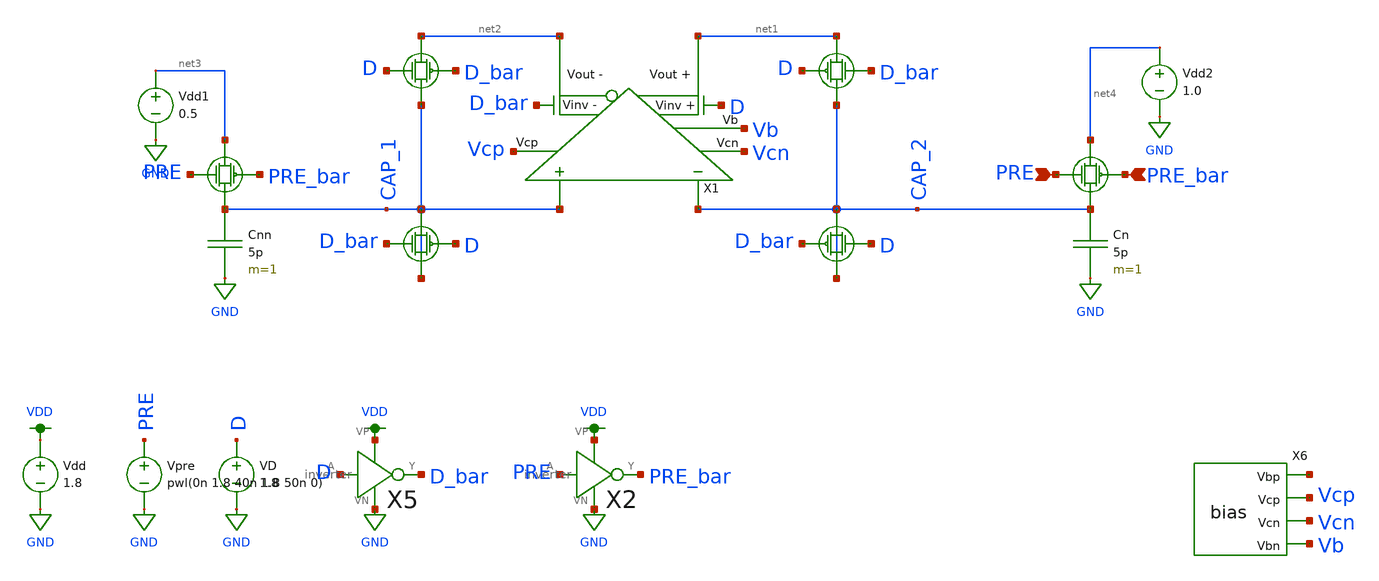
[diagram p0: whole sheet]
** sch_path: simulations/bre_sim.sch
**.subckt bre_sim PRE_bar PRE
*.ipin PRE_bar
*.ipin PRE
X1 D_bar net1 net2 Vcp Vb CAP_2 CAP_1 D Vcn ota W_U=12 L_U=0.5
Cn CAP_2 GND 5p m=1
Cnn CAP_1 GND 5p m=1
Vdd VDD GND 1.8
Vpre PRE GND pwl(0n 1.8 40n 1.8 50n 0)
X2 PRE PRE_bar VDD GND inverter
X5 D D_bar VDD GND inverter
VD D GND 1.8
X6 net5 Vcp Vcn Vb bias
Vdd1 net3 GND 0.5
Vdd2 net4 GND 1.0
**** begin user architecture code

.option wnflag=1
.param MC_SWITCH=0.0
.lib ~/skywater/skywater-pdk/libraries/sky130_fd_pr_ngspice/latest/models/sky130.lib.spice tt


.tran 0.1n 10u
.save all

**** end user architecture code
**.ends

* expanding   symbol:  ../schematics/ota.sym # of pins=9
** sym_path: schematics/ota.sym
** sch_path: schematics/ota.sch
.subckt ota Vinv_n Vout_p Vout_n Vcp Vb Vin_n Vin_p Vinv_p Vcn  L_U=0.5 W_U=12
*.ipin Vin_n
*.ipin Vin_p
*.opin Vout_n
*.opin Vout_p
*.ipin Vcp
*.ipin Vb
*.ipin Vinv_p
*.ipin Vinv_n
*.ipin Vcn
XM18 net3 net3 VDD VDD sky130_fd_pr__pfet_01v8 L=L_U W=W_U nf=1 ad='int((nf+1)/2) * W/nf * 0.29' as='int((nf+2)/2) * W/nf * 0.29'
+ pd='2*int((nf+1)/2) * (W/nf + 0.29)' ps='2*int((nf+2)/2) * (W/nf + 0.29)' nrd='0.29 / W' nrs='0.29 / W'
+ sa=0 sb=0 sd=0 mult=1 m=1
XM19 net4 Vin_n net1 GND sky130_fd_pr__nfet_01v8 L=L_U W=W_U nf=1 ad='int((nf+1)/2) * W/nf * 0.29' as='int((nf+2)/2) * W/nf * 0.29'
+ pd='2*int((nf+1)/2) * (W/nf + 0.29)' ps='2*int((nf+2)/2) * (W/nf + 0.29)' nrd='0.29 / W' nrs='0.29 / W'
+ sa=0 sb=0 sd=0 mult=1 m=1
XM20 net3 Vin_p net1 GND sky130_fd_pr__nfet_01v8 L=L_U W=W_U nf=1 ad='int((nf+1)/2) * W/nf * 0.29' as='int((nf+2)/2) * W/nf * 0.29'
+ pd='2*int((nf+1)/2) * (W/nf + 0.29)' ps='2*int((nf+2)/2) * (W/nf + 0.29)' nrd='0.29 / W' nrs='0.29 / W'
+ sa=0 sb=0 sd=0 mult=1 m=1
XM21 net1 Vb GND GND sky130_fd_pr__nfet_01v8 L=L_U W=W_U nf=1 ad='int((nf+1)/2) * W/nf * 0.29' as='int((nf+2)/2) * W/nf * 0.29'
+ pd='2*int((nf+1)/2) * (W/nf + 0.29)' ps='2*int((nf+2)/2) * (W/nf + 0.29)' nrd='0.29 / W' nrs='0.29 / W'
+ sa=0 sb=0 sd=0 mult=1 m=1
XM22 net4 net4 VDD VDD sky130_fd_pr__pfet_01v8 L=L_U W=W_U nf=1 ad='int((nf+1)/2) * W/nf * 0.29' as='int((nf+2)/2) * W/nf * 0.29'
+ pd='2*int((nf+1)/2) * (W/nf + 0.29)' ps='2*int((nf+2)/2) * (W/nf + 0.29)' nrd='0.29 / W' nrs='0.29 / W'
+ sa=0 sb=0 sd=0 mult=1 m=1
XM23 net7 net3 VDD VDD sky130_fd_pr__pfet_01v8 L=L_U W=W_U nf=1 ad='int((nf+1)/2) * W/nf * 0.29' as='int((nf+2)/2) * W/nf * 0.29'
+ pd='2*int((nf+1)/2) * (W/nf + 0.29)' ps='2*int((nf+2)/2) * (W/nf + 0.29)' nrd='0.29 / W' nrs='0.29 / W'
+ sa=0 sb=0 sd=0 mult=1 m=1
XM24 net8 net4 VDD VDD sky130_fd_pr__pfet_01v8 L=L_U W=W_U nf=1 ad='int((nf+1)/2) * W/nf * 0.29' as='int((nf+2)/2) * W/nf * 0.29'
+ pd='2*int((nf+1)/2) * (W/nf + 0.29)' ps='2*int((nf+2)/2) * (W/nf + 0.29)' nrd='0.29 / W' nrs='0.29 / W'
+ sa=0 sb=0 sd=0 mult=1 m=1
XM25 net8 Vcp Vout_n VDD sky130_fd_pr__pfet_01v8 L=L_U W=W_U nf=1 ad='int((nf+1)/2) * W/nf * 0.29' as='int((nf+2)/2) * W/nf * 0.29'
+ pd='2*int((nf+1)/2) * (W/nf + 0.29)' ps='2*int((nf+2)/2) * (W/nf + 0.29)' nrd='0.29 / W' nrs='0.29 / W'
+ sa=0 sb=0 sd=0 mult=1 m=1
XM26 Vout_p Vcp net7 VDD sky130_fd_pr__pfet_01v8 L=L_U W=W_U nf=1 ad='int((nf+1)/2) * W/nf * 0.29' as='int((nf+2)/2) * W/nf * 0.29'
+ pd='2*int((nf+1)/2) * (W/nf + 0.29)' ps='2*int((nf+2)/2) * (W/nf + 0.29)' nrd='0.29 / W' nrs='0.29 / W'
+ sa=0 sb=0 sd=0 mult=1 m=1
XM27 Vout_p Vcn net6 GND sky130_fd_pr__nfet_01v8 L=L_U W=W_U nf=1 ad='int((nf+1)/2) * W/nf * 0.29' as='int((nf+2)/2) * W/nf * 0.29'
+ pd='2*int((nf+1)/2) * (W/nf + 0.29)' ps='2*int((nf+2)/2) * (W/nf + 0.29)' nrd='0.29 / W' nrs='0.29 / W'
+ sa=0 sb=0 sd=0 mult=1 m=1
XM28 Vout_n Vcn net2 GND sky130_fd_pr__nfet_01v8 L=L_U W=W_U nf=1 ad='int((nf+1)/2) * W/nf * 0.29' as='int((nf+2)/2) * W/nf * 0.29'
+ pd='2*int((nf+1)/2) * (W/nf + 0.29)' ps='2*int((nf+2)/2) * (W/nf + 0.29)' nrd='0.29 / W' nrs='0.29 / W'
+ sa=0 sb=0 sd=0 mult=1 m=1
XM29 net6 net5 GND GND sky130_fd_pr__nfet_01v8 L=L_U W=W_U nf=1 ad='int((nf+1)/2) * W/nf * 0.29' as='int((nf+2)/2) * W/nf * 0.29'
+ pd='2*int((nf+1)/2) * (W/nf + 0.29)' ps='2*int((nf+2)/2) * (W/nf + 0.29)' nrd='0.29 / W' nrs='0.29 / W'
+ sa=0 sb=0 sd=0 mult=1 m=1
XM30 Vout_p Vinv_p net5 GND sky130_fd_pr__nfet_01v8 L=L_U W=W_U nf=1 ad='int((nf+1)/2) * W/nf * 0.29'
+ as='int((nf+2)/2) * W/nf * 0.29' pd='2*int((nf+1)/2) * (W/nf + 0.29)' ps='2*int((nf+2)/2) * (W/nf + 0.29)'
+ nrd='0.29 / W' nrs='0.29 / W' sa=0 sb=0 sd=0 mult=1 m=1
XM32 net2 net5 GND GND sky130_fd_pr__nfet_01v8 L=L_U W=W_U nf=1 ad='int((nf+1)/2) * W/nf * 0.29' as='int((nf+2)/2) * W/nf * 0.29'
+ pd='2*int((nf+1)/2) * (W/nf + 0.29)' ps='2*int((nf+2)/2) * (W/nf + 0.29)' nrd='0.29 / W' nrs='0.29 / W'
+ sa=0 sb=0 sd=0 mult=1 m=1
XM34 Vout_n Vinv_n net5 GND sky130_fd_pr__nfet_01v8 L=L_U W=W_U nf=1 ad='int((nf+1)/2) * W/nf * 0.29'
+ as='int((nf+2)/2) * W/nf * 0.29' pd='2*int((nf+1)/2) * (W/nf + 0.29)' ps='2*int((nf+2)/2) * (W/nf + 0.29)'
+ nrd='0.29 / W' nrs='0.29 / W' sa=0 sb=0 sd=0 mult=1 m=1
.ends


* expanding   symbol:  ../schematics/inverter.sym # of pins=4
** sym_path: schematics/inverter.sym
** sch_path: schematics/inverter.sch
.subckt inverter A Y VP VN
*.ipin A
*.iopin VP
*.iopin VN
*.opin Y
XM1 Y A VP VDD sky130_fd_pr__pfet_01v8 L=0.15 W=1 nf=1 ad='int((nf+1)/2) * W/nf * 0.29' as='int((nf+2)/2) * W/nf * 0.29'
+ pd='2*int((nf+1)/2) * (W/nf + 0.29)' ps='2*int((nf+2)/2) * (W/nf + 0.29)' nrd='0.29 / W' nrs='0.29 / W'
+ sa=0 sb=0 sd=0 mult=1 m=1
XM2 Y A VN GND sky130_fd_pr__nfet_01v8 L=0.15 W=1 nf=1 ad='int((nf+1)/2) * W/nf * 0.29' as='int((nf+2)/2) * W/nf * 0.29'
+ pd='2*int((nf+1)/2) * (W/nf + 0.29)' ps='2*int((nf+2)/2) * (W/nf + 0.29)' nrd='0.29 / W' nrs='0.29 / W'
+ sa=0 sb=0 sd=0 mult=1 m=1
.ends


* expanding   symbol:  ../schematics/bias.sym # of pins=4
** sym_path: schematics/bias.sym
** sch_path: schematics/bias.sch
.subckt bias Vbp Vcp Vcn Vbn
*.opin Vcp
*.opin Vcn
*.opin Vbn
*.opin Vbp
XM1 net1 Vbn GND GND sky130_fd_pr__nfet_01v8 L=2.5 W=12 nf=1 ad='int((nf+1)/2) * W/nf * 0.29' as='int((nf+2)/2) * W/nf * 0.29'
+ pd='2*int((nf+1)/2) * (W/nf + 0.29)' ps='2*int((nf+2)/2) * (W/nf + 0.29)' nrd='0.29 / W' nrs='0.29 / W'
+ sa=0 sb=0 sd=0 mult=1 m=1
XM2 Vcp Vbn GND GND sky130_fd_pr__nfet_01v8 L=0.5 W=12 nf=1 ad='int((nf+1)/2) * W/nf * 0.29' as='int((nf+2)/2) * W/nf * 0.29'
+ pd='2*int((nf+1)/2) * (W/nf + 0.29)' ps='2*int((nf+2)/2) * (W/nf + 0.29)' nrd='0.29 / W' nrs='0.29 / W'
+ sa=0 sb=0 sd=0 mult=1 m=1
XM3 Vbp Vbn GND GND sky130_fd_pr__nfet_01v8 L=0.5 W=12 nf=1 ad='int((nf+1)/2) * W/nf * 0.29' as='int((nf+2)/2) * W/nf * 0.29'
+ pd='2*int((nf+1)/2) * (W/nf + 0.29)' ps='2*int((nf+2)/2) * (W/nf + 0.29)' nrd='0.29 / W' nrs='0.29 / W'
+ sa=0 sb=0 sd=0 mult=1 m=1
XM4 net3 net4 GND GND sky130_fd_pr__nfet_01v8 L=0.5 W=12 nf=1 ad='int((nf+1)/2) * W/nf * 0.29' as='int((nf+2)/2) * W/nf * 0.29'
+ pd='2*int((nf+1)/2) * (W/nf + 0.29)' ps='2*int((nf+2)/2) * (W/nf + 0.29)' nrd='0.29 / W' nrs='0.29 / W'
+ sa=0 sb=0 sd=0 mult=1 m=1
XM5 Vbn Vbn GND GND sky130_fd_pr__nfet_01v8 L=0.5 W=12 nf=1 ad='int((nf+1)/2) * W/nf * 0.29' as='int((nf+2)/2) * W/nf * 0.29'
+ pd='2*int((nf+1)/2) * (W/nf + 0.29)' ps='2*int((nf+2)/2) * (W/nf + 0.29)' nrd='0.29 / W' nrs='0.29 / W'
+ sa=0 sb=0 sd=0 mult=1 m=1
XM6 net4 net4 net3 GND sky130_fd_pr__nfet_01v8 L=0.5 W=48 nf=1 ad='int((nf+1)/2) * W/nf * 0.29' as='int((nf+2)/2) * W/nf * 0.29'
+ pd='2*int((nf+1)/2) * (W/nf + 0.29)' ps='2*int((nf+2)/2) * (W/nf + 0.29)' nrd='0.29 / W' nrs='0.29 / W'
+ sa=0 sb=0 sd=0 mult=1 m=1
XM7 Vcn Vcn net3 GND sky130_fd_pr__nfet_01v8 L=0.5 W=12 nf=1 ad='int((nf+1)/2) * W/nf * 0.29' as='int((nf+2)/2) * W/nf * 0.29'
+ pd='2*int((nf+1)/2) * (W/nf + 0.29)' ps='2*int((nf+2)/2) * (W/nf + 0.29)' nrd='0.29 / W' nrs='0.29 / W'
+ sa=0 sb=0 sd=0 mult=1 m=1
XM8 net1 net1 net2 VDD sky130_fd_pr__pfet_01v8 L=0.5 W=48 nf=1 ad='int((nf+1)/2) * W/nf * 0.29' as='int((nf+2)/2) * W/nf * 0.29'
+ pd='2*int((nf+1)/2) * (W/nf + 0.29)' ps='2*int((nf+2)/2) * (W/nf + 0.29)' nrd='0.29 / W' nrs='0.29 / W'
+ sa=0 sb=0 sd=0 mult=1 m=1
XM9 net2 net1 VDD VDD sky130_fd_pr__pfet_01v8 L=0.5 W=12 nf=1 ad='int((nf+1)/2) * W/nf * 0.29' as='int((nf+2)/2) * W/nf * 0.29'
+ pd='2*int((nf+1)/2) * (W/nf + 0.29)' ps='2*int((nf+2)/2) * (W/nf + 0.29)' nrd='0.29 / W' nrs='0.29 / W'
+ sa=0 sb=0 sd=0 mult=1 m=1
XM10 Vcp Vcp net2 VDD sky130_fd_pr__pfet_01v8 L=0.5 W=12 nf=1 ad='int((nf+1)/2) * W/nf * 0.29' as='int((nf+2)/2) * W/nf * 0.29'
+ pd='2*int((nf+1)/2) * (W/nf + 0.29)' ps='2*int((nf+2)/2) * (W/nf + 0.29)' nrd='0.29 / W' nrs='0.29 / W'
+ sa=0 sb=0 sd=0 mult=1 m=1
XM11 Vbp Vbp VDD VDD sky130_fd_pr__pfet_01v8 L=0.5 W=12 nf=1 ad='int((nf+1)/2) * W/nf * 0.29' as='int((nf+2)/2) * W/nf * 0.29'
+ pd='2*int((nf+1)/2) * (W/nf + 0.29)' ps='2*int((nf+2)/2) * (W/nf + 0.29)' nrd='0.29 / W' nrs='0.29 / W'
+ sa=0 sb=0 sd=0 mult=1 m=1
XM12 net4 Vbp VDD VDD sky130_fd_pr__pfet_01v8 L=2.5 W=12 nf=1 ad='int((nf+1)/2) * W/nf * 0.29' as='int((nf+2)/2) * W/nf * 0.29'
+ pd='2*int((nf+1)/2) * (W/nf + 0.29)' ps='2*int((nf+2)/2) * (W/nf + 0.29)' nrd='0.29 / W' nrs='0.29 / W'
+ sa=0 sb=0 sd=0 mult=1 m=1
XM13 Vcn Vbp VDD VDD sky130_fd_pr__pfet_01v8 L=0.5 W=12 nf=1 ad='int((nf+1)/2) * W/nf * 0.29' as='int((nf+2)/2) * W/nf * 0.29'
+ pd='2*int((nf+1)/2) * (W/nf + 0.29)' ps='2*int((nf+2)/2) * (W/nf + 0.29)' nrd='0.29 / W' nrs='0.29 / W'
+ sa=0 sb=0 sd=0 mult=1 m=1
I1 VDD Vbn 100u
.ends

.GLOBAL GND
.GLOBAL VDD
.end
